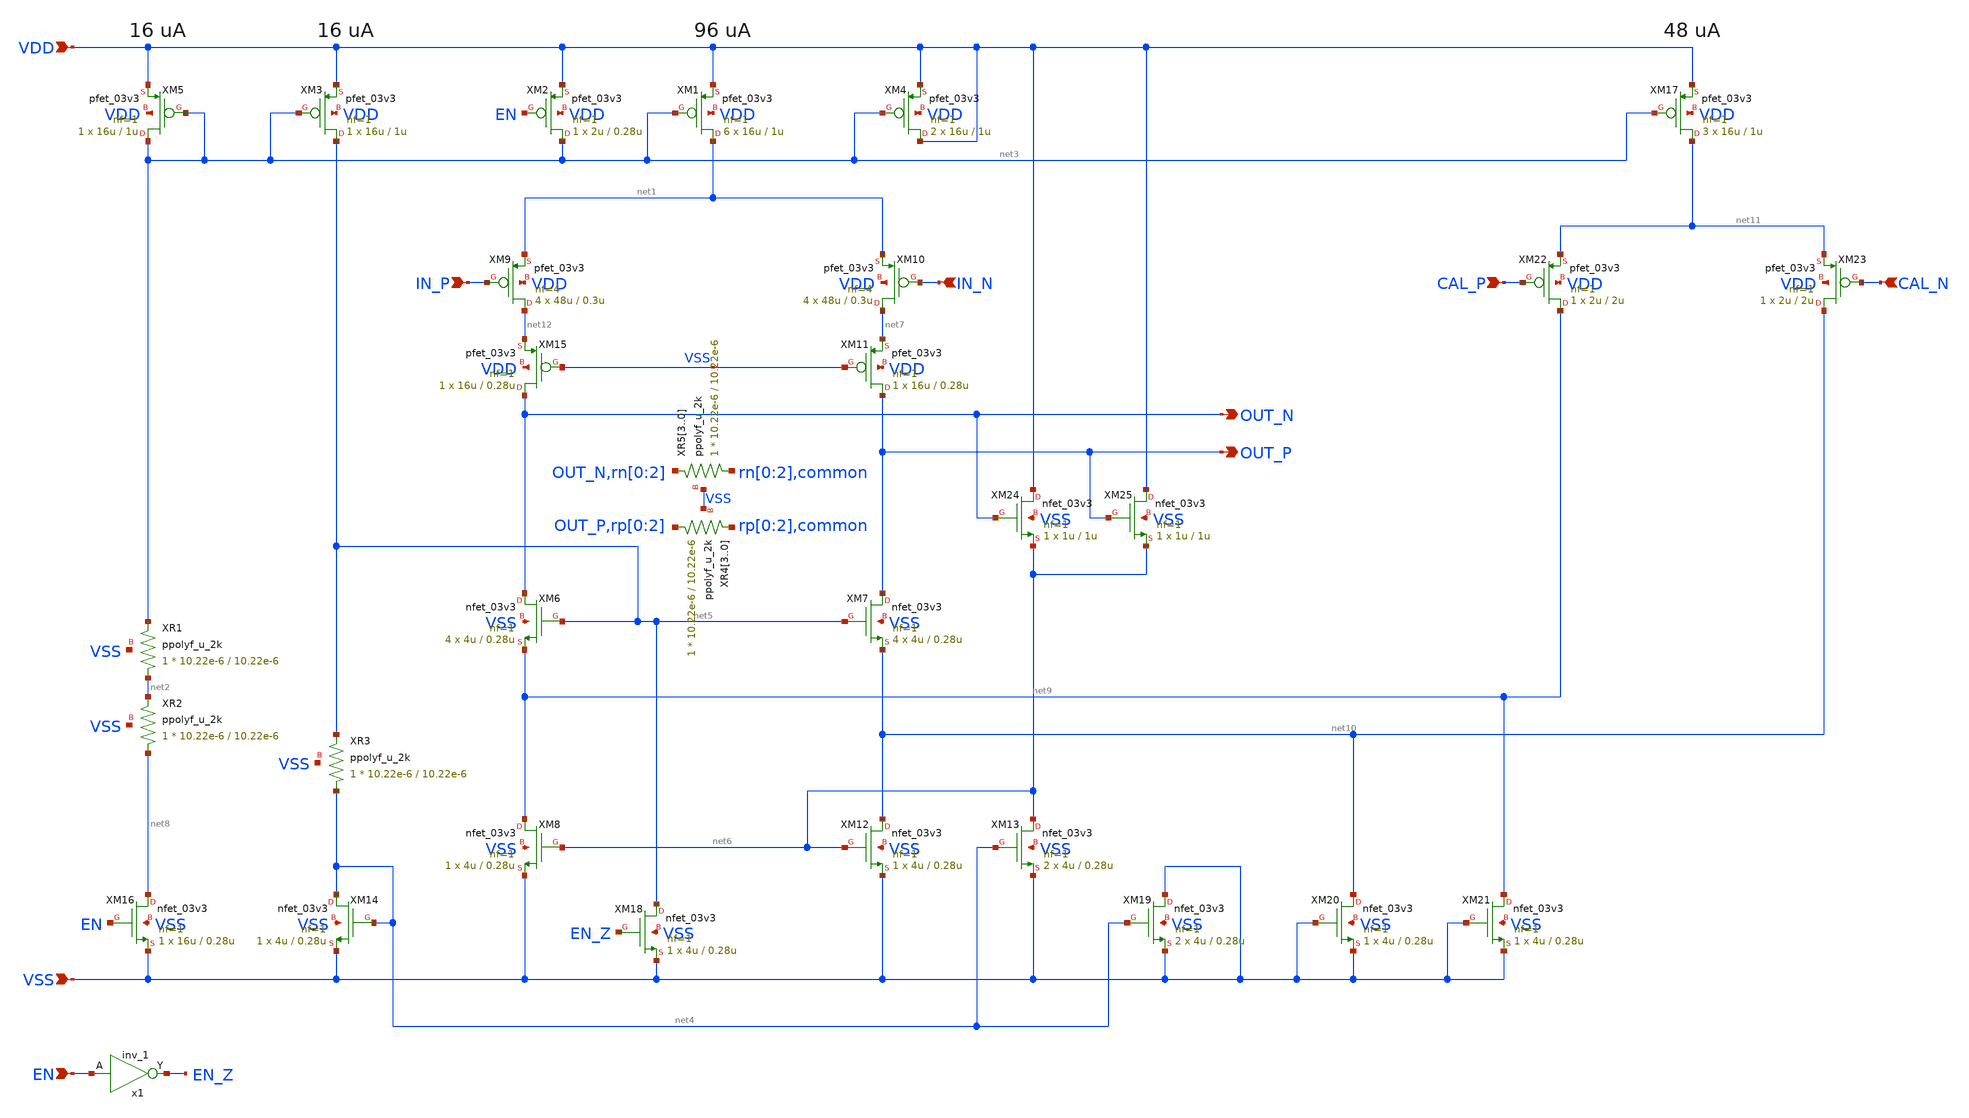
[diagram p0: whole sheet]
** sch_path: Schematic/preamplifier/premplifier.sch
**.subckt premplifier VDD VSS IN_P IN_N OUT_P OUT_N EN CAL_P CAL_N
*.ipin VDD
*.ipin VSS
*.ipin IN_P
*.ipin IN_N
*.opin OUT_P
*.opin OUT_N
*.ipin EN
*.ipin CAL_P
*.ipin CAL_N
x1 EN VGND VNB VPB VPWR EN_Z gf180mcu_fd_sc_mcu7t5v0__inv_1
XM3 net5 net3 VDD VDD pfet_03v3 L=1u W=16u nf=1 ad='int((nf+1)/2) * W/nf * 0.18u' as='int((nf+2)/2) * W/nf * 0.18u'
+ pd='2*int((nf+1)/2) * (W/nf + 0.18u)' ps='2*int((nf+2)/2) * (W/nf + 0.18u)' nrd='0.18u / W' nrs='0.18u / W'
+ sa=0 sb=0 sd=0 m=1
XM5 net3 net3 VDD VDD pfet_03v3 L=1u W=16u nf=1 ad='int((nf+1)/2) * W/nf * 0.18u' as='int((nf+2)/2) * W/nf * 0.18u'
+ pd='2*int((nf+1)/2) * (W/nf + 0.18u)' ps='2*int((nf+2)/2) * (W/nf + 0.18u)' nrd='0.18u / W' nrs='0.18u / W'
+ sa=0 sb=0 sd=0 m=1
XM1 net1 net3 VDD VDD pfet_03v3 L=1u W=16u nf=1 ad='int((nf+1)/2) * W/nf * 0.18u' as='int((nf+2)/2) * W/nf * 0.18u'
+ pd='2*int((nf+1)/2) * (W/nf + 0.18u)' ps='2*int((nf+2)/2) * (W/nf + 0.18u)' nrd='0.18u / W' nrs='0.18u / W'
+ sa=0 sb=0 sd=0 m=6
XM2 net3 EN VDD VDD pfet_03v3 L=0.28u W=2u nf=1 ad='int((nf+1)/2) * W/nf * 0.18u' as='int((nf+2)/2) * W/nf * 0.18u'
+ pd='2*int((nf+1)/2) * (W/nf + 0.18u)' ps='2*int((nf+2)/2) * (W/nf + 0.18u)' nrd='0.18u / W' nrs='0.18u / W'
+ sa=0 sb=0 sd=0 m=1
XM4 VDD net3 VDD VDD pfet_03v3 L=1u W=16u nf=1 ad='int((nf+1)/2) * W/nf * 0.18u' as='int((nf+2)/2) * W/nf * 0.18u'
+ pd='2*int((nf+1)/2) * (W/nf + 0.18u)' ps='2*int((nf+2)/2) * (W/nf + 0.18u)' nrd='0.18u / W' nrs='0.18u / W'
+ sa=0 sb=0 sd=0 m=2
XM9 net12 IN_P net1 VDD pfet_03v3 L=0.3u W=48u nf=4 ad='int((nf+1)/2) * W/nf * 0.18u' as='int((nf+2)/2) * W/nf * 0.18u'
+ pd='2*int((nf+1)/2) * (W/nf + 0.18u)' ps='2*int((nf+2)/2) * (W/nf + 0.18u)' nrd='0.18u / W' nrs='0.18u / W'
+ sa=0 sb=0 sd=0 m=4
XM10 net7 IN_N net1 VDD pfet_03v3 L=0.3u W=48u nf=4 ad='int((nf+1)/2) * W/nf * 0.18u' as='int((nf+2)/2) * W/nf * 0.18u'
+ pd='2*int((nf+1)/2) * (W/nf + 0.18u)' ps='2*int((nf+2)/2) * (W/nf + 0.18u)' nrd='0.18u / W' nrs='0.18u / W'
+ sa=0 sb=0 sd=0 m=4
XM11 OUT_P VSS net7 VDD pfet_03v3 L=0.28u W=16u nf=1 ad='int((nf+1)/2) * W/nf * 0.18u' as='int((nf+2)/2) * W/nf * 0.18u'
+ pd='2*int((nf+1)/2) * (W/nf + 0.18u)' ps='2*int((nf+2)/2) * (W/nf + 0.18u)' nrd='0.18u / W' nrs='0.18u / W'
+ sa=0 sb=0 sd=0 m=1
XM15 OUT_N VSS net12 VDD pfet_03v3 L=0.28u W=16u nf=1 ad='int((nf+1)/2) * W/nf * 0.18u' as='int((nf+2)/2) * W/nf * 0.18u'
+ pd='2*int((nf+1)/2) * (W/nf + 0.18u)' ps='2*int((nf+2)/2) * (W/nf + 0.18u)' nrd='0.18u / W' nrs='0.18u / W'
+ sa=0 sb=0 sd=0 m=1
XM17 net11 net3 VDD VDD pfet_03v3 L=1u W=16u nf=1 ad='int((nf+1)/2) * W/nf * 0.18u' as='int((nf+2)/2) * W/nf * 0.18u'
+ pd='2*int((nf+1)/2) * (W/nf + 0.18u)' ps='2*int((nf+2)/2) * (W/nf + 0.18u)' nrd='0.18u / W' nrs='0.18u / W'
+ sa=0 sb=0 sd=0 m=3
XM22 net9 CAL_P net11 VDD pfet_03v3 L=2u W=2u nf=1 ad='int((nf+1)/2) * W/nf * 0.18u' as='int((nf+2)/2) * W/nf * 0.18u'
+ pd='2*int((nf+1)/2) * (W/nf + 0.18u)' ps='2*int((nf+2)/2) * (W/nf + 0.18u)' nrd='0.18u / W' nrs='0.18u / W'
+ sa=0 sb=0 sd=0 m=1
XM23 net10 CAL_N net11 VDD pfet_03v3 L=2u W=2u nf=1 ad='int((nf+1)/2) * W/nf * 0.18u' as='int((nf+2)/2) * W/nf * 0.18u'
+ pd='2*int((nf+1)/2) * (W/nf + 0.18u)' ps='2*int((nf+2)/2) * (W/nf + 0.18u)' nrd='0.18u / W' nrs='0.18u / W'
+ sa=0 sb=0 sd=0 m=1
XM6 OUT_N net5 net9 VSS nfet_03v3 L=0.28u W=4u nf=1 ad='int((nf+1)/2) * W/nf * 0.18u' as='int((nf+2)/2) * W/nf * 0.18u'
+ pd='2*int((nf+1)/2) * (W/nf + 0.18u)' ps='2*int((nf+2)/2) * (W/nf + 0.18u)' nrd='0.18u / W' nrs='0.18u / W'
+ sa=0 sb=0 sd=0 m=4
XM7 OUT_P net5 net10 VSS nfet_03v3 L=0.28u W=4u nf=1 ad='int((nf+1)/2) * W/nf * 0.18u' as='int((nf+2)/2) * W/nf * 0.18u'
+ pd='2*int((nf+1)/2) * (W/nf + 0.18u)' ps='2*int((nf+2)/2) * (W/nf + 0.18u)' nrd='0.18u / W' nrs='0.18u / W'
+ sa=0 sb=0 sd=0 m=4
XM8 net9 net6 VSS VSS nfet_03v3 L=0.28u W=4u nf=1 ad='int((nf+1)/2) * W/nf * 0.18u' as='int((nf+2)/2) * W/nf * 0.18u'
+ pd='2*int((nf+1)/2) * (W/nf + 0.18u)' ps='2*int((nf+2)/2) * (W/nf + 0.18u)' nrd='0.18u / W' nrs='0.18u / W'
+ sa=0 sb=0 sd=0 m=1
XM12 net10 net6 VSS VSS nfet_03v3 L=0.28u W=4u nf=1 ad='int((nf+1)/2) * W/nf * 0.18u' as='int((nf+2)/2) * W/nf * 0.18u'
+ pd='2*int((nf+1)/2) * (W/nf + 0.18u)' ps='2*int((nf+2)/2) * (W/nf + 0.18u)' nrd='0.18u / W' nrs='0.18u / W'
+ sa=0 sb=0 sd=0 m=1
XM13 net6 net4 VSS VSS nfet_03v3 L=0.28u W=4u nf=1 ad='int((nf+1)/2) * W/nf * 0.18u' as='int((nf+2)/2) * W/nf * 0.18u'
+ pd='2*int((nf+1)/2) * (W/nf + 0.18u)' ps='2*int((nf+2)/2) * (W/nf + 0.18u)' nrd='0.18u / W' nrs='0.18u / W'
+ sa=0 sb=0 sd=0 m=2
XM14 net4 net4 VSS VSS nfet_03v3 L=0.28u W=4u nf=1 ad='int((nf+1)/2) * W/nf * 0.18u' as='int((nf+2)/2) * W/nf * 0.18u'
+ pd='2*int((nf+1)/2) * (W/nf + 0.18u)' ps='2*int((nf+2)/2) * (W/nf + 0.18u)' nrd='0.18u / W' nrs='0.18u / W'
+ sa=0 sb=0 sd=0 m=1
XM16 net8 EN VSS VSS nfet_03v3 L=0.28u W=16u nf=1 ad='int((nf+1)/2) * W/nf * 0.18u' as='int((nf+2)/2) * W/nf * 0.18u'
+ pd='2*int((nf+1)/2) * (W/nf + 0.18u)' ps='2*int((nf+2)/2) * (W/nf + 0.18u)' nrd='0.18u / W' nrs='0.18u / W'
+ sa=0 sb=0 sd=0 m=1
XM18 net5 EN_Z VSS VSS nfet_03v3 L=0.28u W=4u nf=1 ad='int((nf+1)/2) * W/nf * 0.18u' as='int((nf+2)/2) * W/nf * 0.18u'
+ pd='2*int((nf+1)/2) * (W/nf + 0.18u)' ps='2*int((nf+2)/2) * (W/nf + 0.18u)' nrd='0.18u / W' nrs='0.18u / W'
+ sa=0 sb=0 sd=0 m=1
XM19 VSS net4 VSS VSS nfet_03v3 L=0.28u W=4u nf=1 ad='int((nf+1)/2) * W/nf * 0.18u' as='int((nf+2)/2) * W/nf * 0.18u'
+ pd='2*int((nf+1)/2) * (W/nf + 0.18u)' ps='2*int((nf+2)/2) * (W/nf + 0.18u)' nrd='0.18u / W' nrs='0.18u / W'
+ sa=0 sb=0 sd=0 m=2
XM20 net10 VSS VSS VSS nfet_03v3 L=0.28u W=4u nf=1 ad='int((nf+1)/2) * W/nf * 0.18u' as='int((nf+2)/2) * W/nf * 0.18u'
+ pd='2*int((nf+1)/2) * (W/nf + 0.18u)' ps='2*int((nf+2)/2) * (W/nf + 0.18u)' nrd='0.18u / W' nrs='0.18u / W'
+ sa=0 sb=0 sd=0 m=1
XM21 net9 VSS VSS VSS nfet_03v3 L=0.28u W=4u nf=1 ad='int((nf+1)/2) * W/nf * 0.18u' as='int((nf+2)/2) * W/nf * 0.18u'
+ pd='2*int((nf+1)/2) * (W/nf + 0.18u)' ps='2*int((nf+2)/2) * (W/nf + 0.18u)' nrd='0.18u / W' nrs='0.18u / W'
+ sa=0 sb=0 sd=0 m=1
XM24 VDD OUT_N net6 VSS nfet_03v3 L=1u W=1u nf=1 ad='int((nf+1)/2) * W/nf * 0.18u' as='int((nf+2)/2) * W/nf * 0.18u'
+ pd='2*int((nf+1)/2) * (W/nf + 0.18u)' ps='2*int((nf+2)/2) * (W/nf + 0.18u)' nrd='0.18u / W' nrs='0.18u / W'
+ sa=0 sb=0 sd=0 m=1
XM25 VDD OUT_P net6 VSS nfet_03v3 L=1u W=1u nf=1 ad='int((nf+1)/2) * W/nf * 0.18u' as='int((nf+2)/2) * W/nf * 0.18u'
+ pd='2*int((nf+1)/2) * (W/nf + 0.18u)' ps='2*int((nf+2)/2) * (W/nf + 0.18u)' nrd='0.18u / W' nrs='0.18u / W'
+ sa=0 sb=0 sd=0 m=1
XR1 net2 net3 VSS ppolyf_u_2k r_width=10.22e-6 r_length=10.22e-6 m=1
XR2 net8 net2 VSS ppolyf_u_2k r_width=10.22e-6 r_length=10.22e-6 m=1
XR3 net4 net5 VSS ppolyf_u_2k r_width=10.22e-6 r_length=10.22e-6 m=1
XR43 OUT_P rp[0] VSS ppolyf_u_2k r_width=10.22e-6 r_length=10.22e-6 m=1
XR42 rp[0] rp[1] VSS ppolyf_u_2k r_width=10.22e-6 r_length=10.22e-6 m=1
XR41 rp[1] rp[2] VSS ppolyf_u_2k r_width=10.22e-6 r_length=10.22e-6 m=1
XR40 rp[2] common VSS ppolyf_u_2k r_width=10.22e-6 r_length=10.22e-6 m=1
XR53 rn[0] OUT_N VSS ppolyf_u_2k r_width=10.22e-6 r_length=10.22e-6 m=1
XR52 rn[1] rn[0] VSS ppolyf_u_2k r_width=10.22e-6 r_length=10.22e-6 m=1
XR51 rn[2] rn[1] VSS ppolyf_u_2k r_width=10.22e-6 r_length=10.22e-6 m=1
XR50 common rn[2] VSS ppolyf_u_2k r_width=10.22e-6 r_length=10.22e-6 m=1
**.ends
.end
